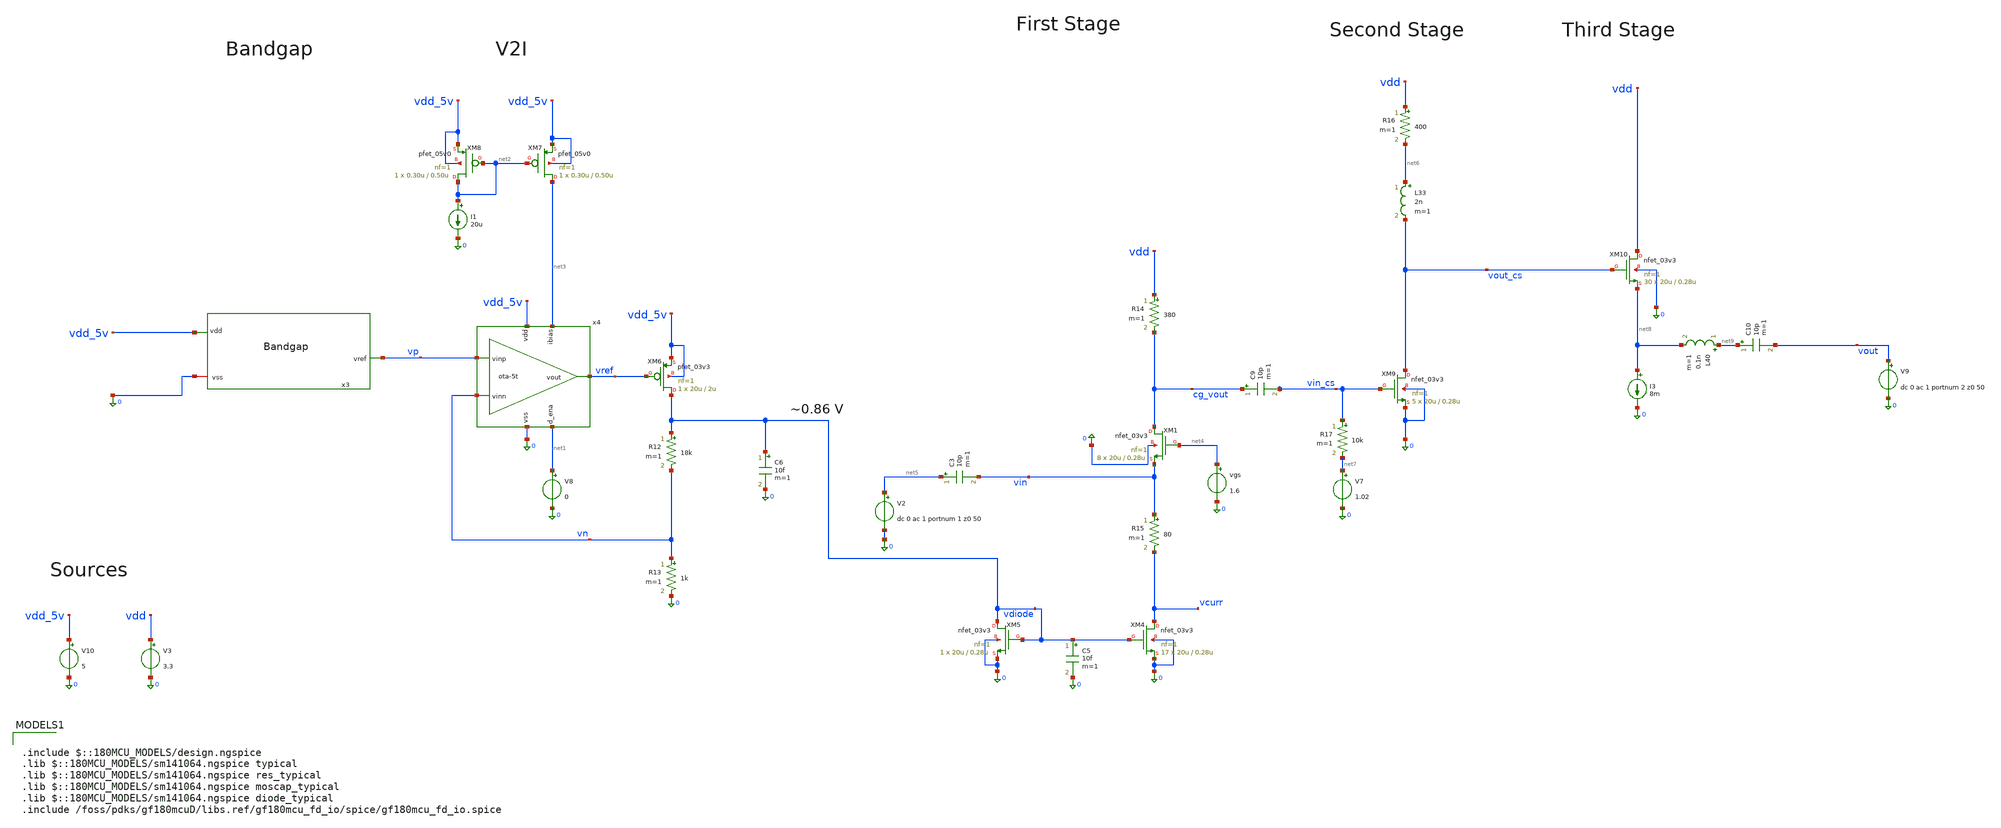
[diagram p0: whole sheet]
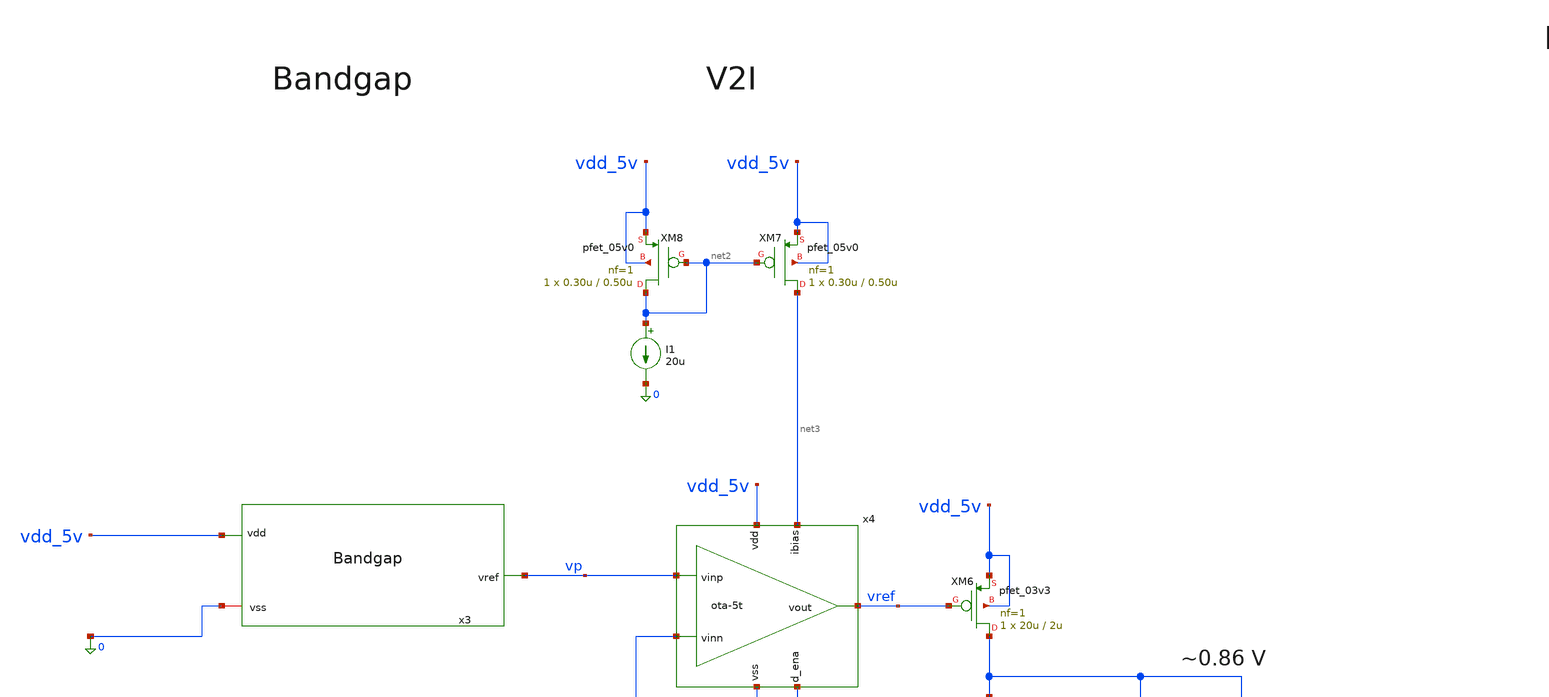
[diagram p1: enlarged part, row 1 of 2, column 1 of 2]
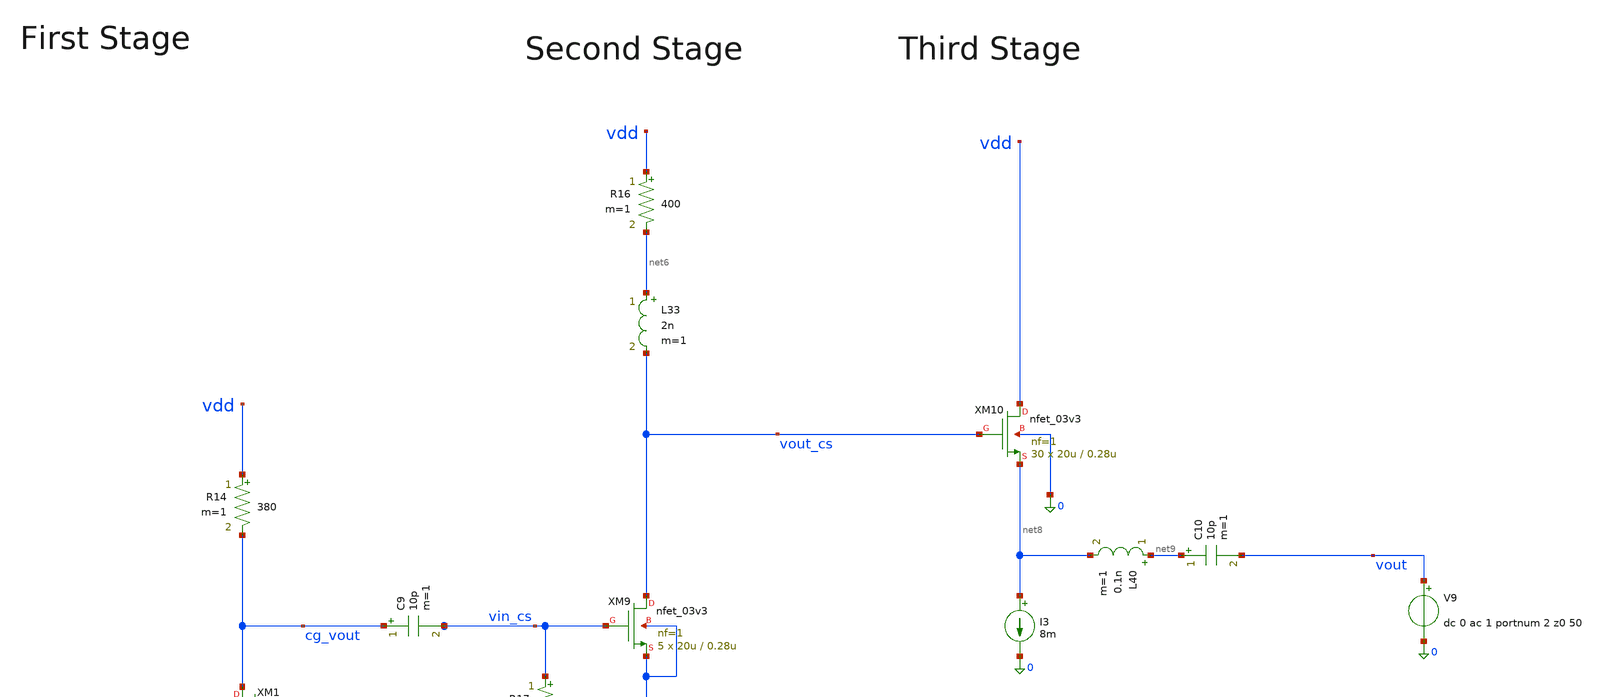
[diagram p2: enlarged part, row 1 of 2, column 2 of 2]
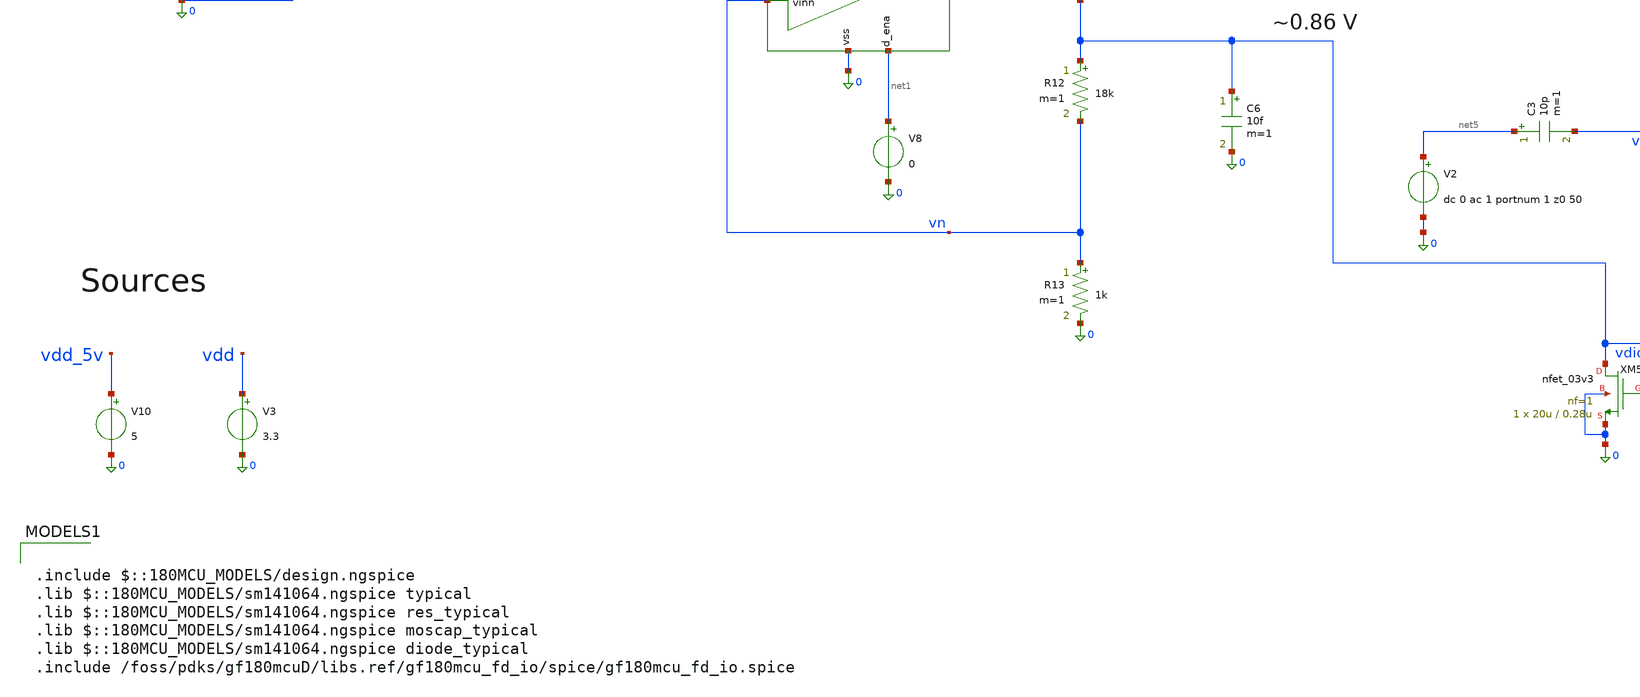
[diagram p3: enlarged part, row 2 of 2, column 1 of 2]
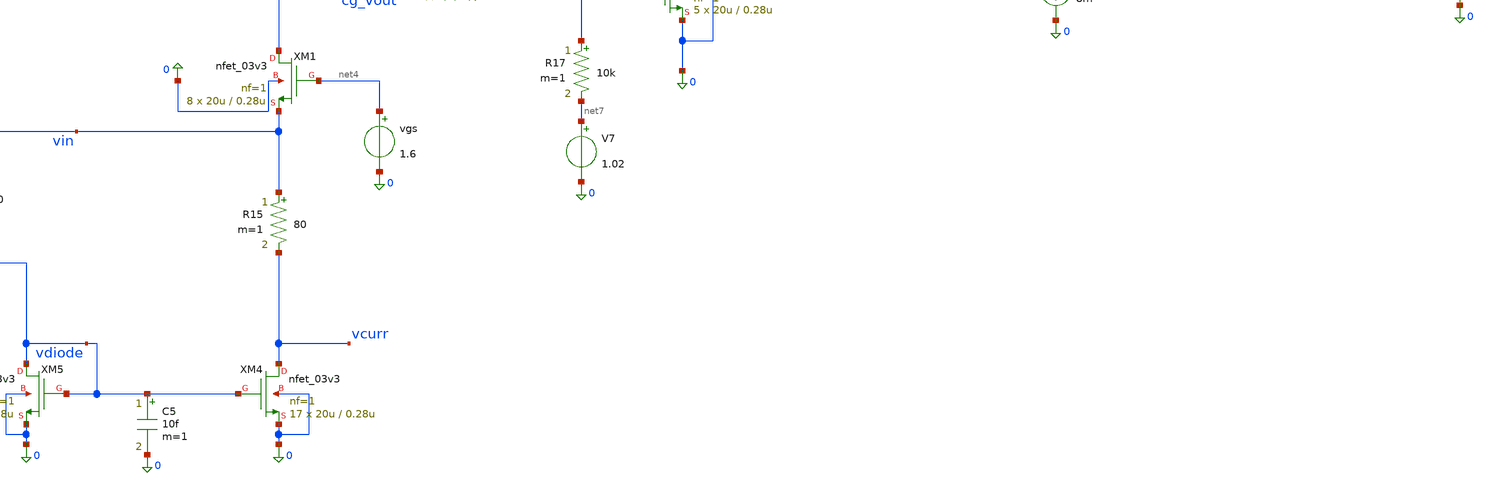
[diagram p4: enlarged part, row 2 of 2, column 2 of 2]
** sch_path: xschem_dev_ghaith_lowtailnoise/LNA_sim.sch
**.subckt LNA_sim
x3 vdd_5v vp 0 bandgap
x4 vdd_5v vref vp vn net3 net1 0 ota-5t
V8 net1 0 0
I1 net2 0 20u
XM6 vdiode vref vdd_5v vdd_5v pfet_03v3 L=2u W=20u nf=1 ad='int((nf+1)/2) * W/nf * 0.18u' as='int((nf+2)/2) * W/nf * 0.18u'
+ pd='2*int((nf+1)/2) * (W/nf + 0.18u)' ps='2*int((nf+2)/2) * (W/nf + 0.18u)' nrd='0.18u / W' nrs='0.18u / W'
+ sa=0 sb=0 sd=0 m=1
R12 vdiode vn 18k m=1
R13 vn 0 1k m=1
C6 vdiode 0 10f m=1
XM7 net3 net2 vdd_5v vdd_5v pfet_05v0 L=0.50u W=0.30u nf=1 ad='int((nf+1)/2) * W/nf * 0.18u' as='int((nf+2)/2) * W/nf * 0.18u'
+ pd='2*int((nf+1)/2) * (W/nf + 0.18u)' ps='2*int((nf+2)/2) * (W/nf + 0.18u)' nrd='0.18u / W' nrs='0.18u / W'
+ sa=0 sb=0 sd=0 m=1
XM8 net2 net2 vdd_5v vdd_5v pfet_05v0 L=0.50u W=0.30u nf=1 ad='int((nf+1)/2) * W/nf * 0.18u' as='int((nf+2)/2) * W/nf * 0.18u'
+ pd='2*int((nf+1)/2) * (W/nf + 0.18u)' ps='2*int((nf+2)/2) * (W/nf + 0.18u)' nrd='0.18u / W' nrs='0.18u / W'
+ sa=0 sb=0 sd=0 m=1
V3 vdd 0 3.3
V10 vdd_5v 0 5
vgs net4 0 1.6
R14 vdd cg_vout 380 m=1
XM1 cg_vout net4 vin 0 nfet_03v3 L=0.28u W=20u nf=1 ad='int((nf+1)/2) * W/nf * 0.18u' as='int((nf+2)/2) * W/nf * 0.18u'
+ pd='2*int((nf+1)/2) * (W/nf + 0.18u)' ps='2*int((nf+2)/2) * (W/nf + 0.18u)' nrd='0.18u / W' nrs='0.18u / W'
+ sa=0 sb=0 sd=0 m=8
V2 net5 0 dc 0 ac 1 portnum 1 z0 50
XM4 vcurr vdiode 0 0 nfet_03v3 L=0.28u W=20u nf=1 ad='int((nf+1)/2) * W/nf * 0.18u' as='int((nf+2)/2) * W/nf * 0.18u'
+ pd='2*int((nf+1)/2) * (W/nf + 0.18u)' ps='2*int((nf+2)/2) * (W/nf + 0.18u)' nrd='0.18u / W' nrs='0.18u / W'
+ sa=0 sb=0 sd=0 m=17
C3 net5 vin 10p m=1
R15 vin vcurr 80 m=1
XM5 vdiode vdiode 0 0 nfet_03v3 L=0.28u W=20u nf=1 ad='int((nf+1)/2) * W/nf * 0.18u' as='int((nf+2)/2) * W/nf * 0.18u'
+ pd='2*int((nf+1)/2) * (W/nf + 0.18u)' ps='2*int((nf+2)/2) * (W/nf + 0.18u)' nrd='0.18u / W' nrs='0.18u / W'
+ sa=0 sb=0 sd=0 m=1
C5 vdiode 0 10f m=1
C9 cg_vout vin_cs 10p m=1
XM9 vout_cs vin_cs 0 0 nfet_03v3 L=0.28u W=20u nf=1 ad='int((nf+1)/2) * W/nf * 0.18u' as='int((nf+2)/2) * W/nf * 0.18u'
+ pd='2*int((nf+1)/2) * (W/nf + 0.18u)' ps='2*int((nf+2)/2) * (W/nf + 0.18u)' nrd='0.18u / W' nrs='0.18u / W'
+ sa=0 sb=0 sd=0 m=5
R16 vdd net6 400 m=1
V7 net7 0 1.02
L33 net6 vout_cs 2n m=1
R17 vin_cs net7 10k m=1
V9 vout 0 dc 0 ac 1 portnum 2 z0 50
XM10 vdd vout_cs net8 0 nfet_03v3 L=0.28u W=20u nf=1 ad='int((nf+1)/2) * W/nf * 0.18u' as='int((nf+2)/2) * W/nf * 0.18u'
+ pd='2*int((nf+1)/2) * (W/nf + 0.18u)' ps='2*int((nf+2)/2) * (W/nf + 0.18u)' nrd='0.18u / W' nrs='0.18u / W'
+ sa=0 sb=0 sd=0 m=30
I3 net8 0 8m
C10 net9 vout 10p m=1
L40 net9 net8 0.1n m=1
**** begin user architecture code

.include $::180MCU_MODELS/design.ngspice
.lib $::180MCU_MODELS/sm141064.ngspice typical
.lib $::180MCU_MODELS/sm141064.ngspice res_typical
.lib $::180MCU_MODELS/sm141064.ngspice moscap_typical
.lib $::180MCU_MODELS/sm141064.ngspice diode_typical
.include /foss/pdks/gf180mcuD/libs.ref/gf180mcu_fd_io/spice/gf180mcu_fd_io.spice


.include $::180MCU_MODELS/design.ngspice
.lib $::180MCU_MODELS/sm141064.ngspice bjt_typical





.temp 25

.control

*need it, if a loop simulation
*set spnum = 1

sp lin 500 100e6 10e9 1
write LNA_sim.raw


let zin = 50*(1+s_1_1)/(1-s_1_1)
plot mag(zin)
plot ph(zin)

plot vdb(s_1_1) vdb(s_2_2)
plot vdb(s_2_1)
plot nf NFmin
plot Im(zin) Re(zin)



.endc


**** end user architecture code
**.ends
.end
